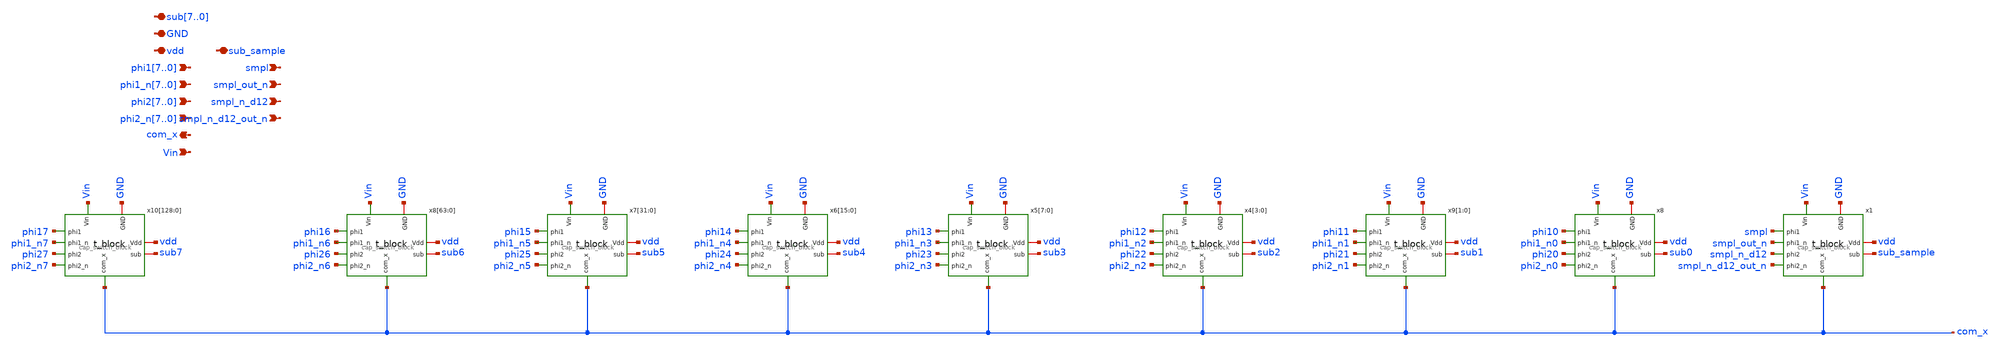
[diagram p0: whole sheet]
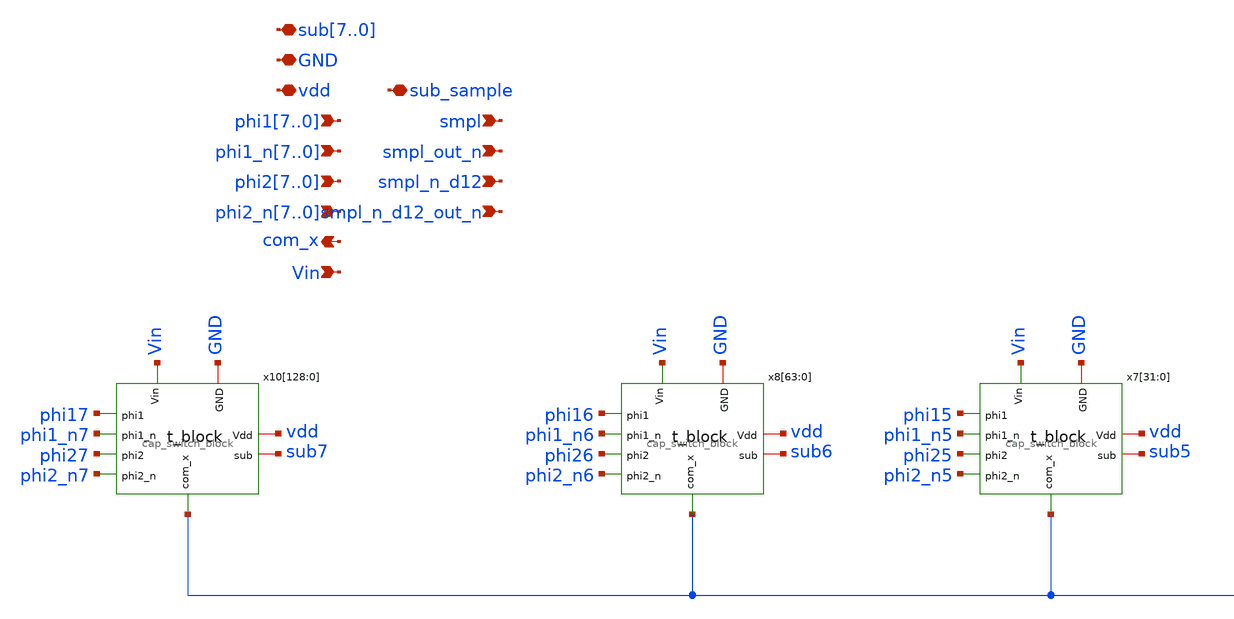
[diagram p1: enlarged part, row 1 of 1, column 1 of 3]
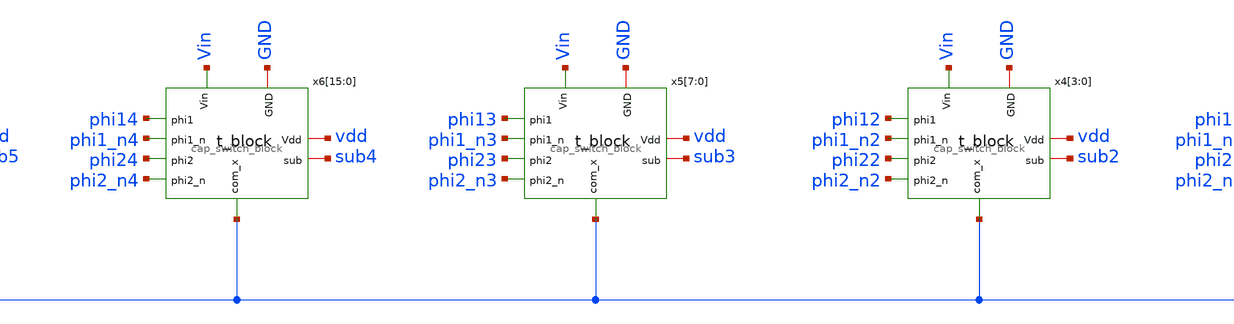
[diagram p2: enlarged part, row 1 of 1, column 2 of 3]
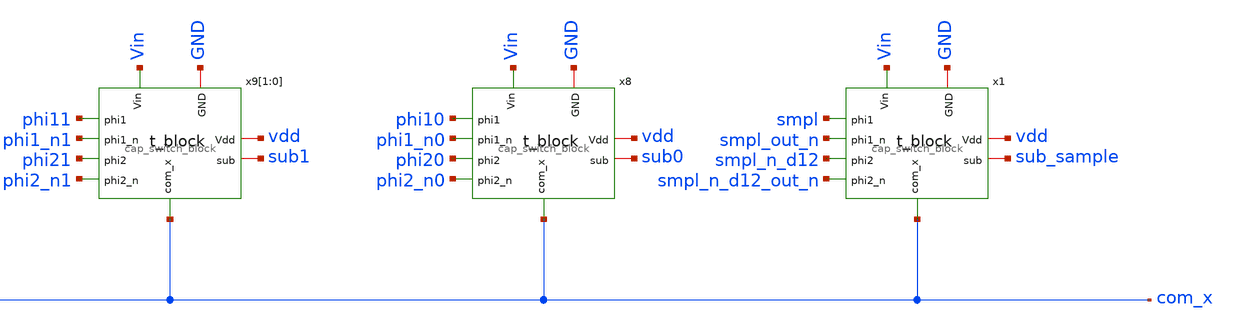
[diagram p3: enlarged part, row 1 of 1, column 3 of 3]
** sch_path: test/design/capblock_256.sch
**.subckt capblock_256 phi17,phi16,phi15,phi14,phi13,phi12,phi11,phi10
*+ phi1_n7,phi1_n6,phi1_n5,phi1_n4,phi1_n3,phi1_n2,phi1_n1,phi1_n0 vdd GND sub7,sub6,sub5,sub4,sub3,sub2,sub1,sub0 phi27,phi26,phi25,phi24,phi23,phi22,phi21,phi20
*+ phi2_n7,phi2_n6,phi2_n5,phi2_n4,phi2_n3,phi2_n2,phi2_n1,phi2_n0 Vin com_x smpl smpl_out_n smpl_n_d12 smpl_n_d12_out_n sub_sample
*.ipin phi17,phi16,phi15,phi14,phi13,phi12,phi11,phi10
*.ipin phi1_n7,phi1_n6,phi1_n5,phi1_n4,phi1_n3,phi1_n2,phi1_n1,phi1_n0
*.iopin vdd
*.iopin GND
*.iopin sub7,sub6,sub5,sub4,sub3,sub2,sub1,sub0
*.ipin phi27,phi26,phi25,phi24,phi23,phi22,phi21,phi20
*.ipin phi2_n7,phi2_n6,phi2_n5,phi2_n4,phi2_n3,phi2_n2,phi2_n1,phi2_n0
*.ipin Vin
*.opin com_x
*.ipin smpl
*.ipin smpl_out_n
*.ipin smpl_n_d12
*.ipin smpl_n_d12_out_n
*.iopin sub_sample
x8 Vin sub0 GND vdd phi10 phi20 phi2_n0 phi1_n0 com_x cap_switch_block
x9[1] Vin sub1 GND vdd phi11 phi21 phi2_n1 phi1_n1 com_x cap_switch_block
x9[0] Vin sub1 GND vdd phi11 phi21 phi2_n1 phi1_n1 com_x cap_switch_block
x4[3] Vin sub2 GND vdd phi12 phi22 phi2_n2 phi1_n2 com_x cap_switch_block
x4[2] Vin sub2 GND vdd phi12 phi22 phi2_n2 phi1_n2 com_x cap_switch_block
x4[1] Vin sub2 GND vdd phi12 phi22 phi2_n2 phi1_n2 com_x cap_switch_block
x4[0] Vin sub2 GND vdd phi12 phi22 phi2_n2 phi1_n2 com_x cap_switch_block
x5[7] Vin sub3 GND vdd phi13 phi23 phi2_n3 phi1_n3 com_x cap_switch_block
x5[6] Vin sub3 GND vdd phi13 phi23 phi2_n3 phi1_n3 com_x cap_switch_block
x5[5] Vin sub3 GND vdd phi13 phi23 phi2_n3 phi1_n3 com_x cap_switch_block
x5[4] Vin sub3 GND vdd phi13 phi23 phi2_n3 phi1_n3 com_x cap_switch_block
x5[3] Vin sub3 GND vdd phi13 phi23 phi2_n3 phi1_n3 com_x cap_switch_block
x5[2] Vin sub3 GND vdd phi13 phi23 phi2_n3 phi1_n3 com_x cap_switch_block
x5[1] Vin sub3 GND vdd phi13 phi23 phi2_n3 phi1_n3 com_x cap_switch_block
x5[0] Vin sub3 GND vdd phi13 phi23 phi2_n3 phi1_n3 com_x cap_switch_block
x6[15] Vin sub4 GND vdd phi14 phi24 phi2_n4 phi1_n4 com_x cap_switch_block
x6[14] Vin sub4 GND vdd phi14 phi24 phi2_n4 phi1_n4 com_x cap_switch_block
x6[13] Vin sub4 GND vdd phi14 phi24 phi2_n4 phi1_n4 com_x cap_switch_block
x6[12] Vin sub4 GND vdd phi14 phi24 phi2_n4 phi1_n4 com_x cap_switch_block
x6[11] Vin sub4 GND vdd phi14 phi24 phi2_n4 phi1_n4 com_x cap_switch_block
x6[10] Vin sub4 GND vdd phi14 phi24 phi2_n4 phi1_n4 com_x cap_switch_block
x6[9] Vin sub4 GND vdd phi14 phi24 phi2_n4 phi1_n4 com_x cap_switch_block
x6[8] Vin sub4 GND vdd phi14 phi24 phi2_n4 phi1_n4 com_x cap_switch_block
x6[7] Vin sub4 GND vdd phi14 phi24 phi2_n4 phi1_n4 com_x cap_switch_block
x6[6] Vin sub4 GND vdd phi14 phi24 phi2_n4 phi1_n4 com_x cap_switch_block
x6[5] Vin sub4 GND vdd phi14 phi24 phi2_n4 phi1_n4 com_x cap_switch_block
x6[4] Vin sub4 GND vdd phi14 phi24 phi2_n4 phi1_n4 com_x cap_switch_block
x6[3] Vin sub4 GND vdd phi14 phi24 phi2_n4 phi1_n4 com_x cap_switch_block
x6[2] Vin sub4 GND vdd phi14 phi24 phi2_n4 phi1_n4 com_x cap_switch_block
x6[1] Vin sub4 GND vdd phi14 phi24 phi2_n4 phi1_n4 com_x cap_switch_block
x6[0] Vin sub4 GND vdd phi14 phi24 phi2_n4 phi1_n4 com_x cap_switch_block
x7[31] Vin sub5 GND vdd phi15 phi25 phi2_n5 phi1_n5 com_x cap_switch_block
x7[30] Vin sub5 GND vdd phi15 phi25 phi2_n5 phi1_n5 com_x cap_switch_block
x7[29] Vin sub5 GND vdd phi15 phi25 phi2_n5 phi1_n5 com_x cap_switch_block
x7[28] Vin sub5 GND vdd phi15 phi25 phi2_n5 phi1_n5 com_x cap_switch_block
x7[27] Vin sub5 GND vdd phi15 phi25 phi2_n5 phi1_n5 com_x cap_switch_block
x7[26] Vin sub5 GND vdd phi15 phi25 phi2_n5 phi1_n5 com_x cap_switch_block
x7[25] Vin sub5 GND vdd phi15 phi25 phi2_n5 phi1_n5 com_x cap_switch_block
x7[24] Vin sub5 GND vdd phi15 phi25 phi2_n5 phi1_n5 com_x cap_switch_block
x7[23] Vin sub5 GND vdd phi15 phi25 phi2_n5 phi1_n5 com_x cap_switch_block
x7[22] Vin sub5 GND vdd phi15 phi25 phi2_n5 phi1_n5 com_x cap_switch_block
x7[21] Vin sub5 GND vdd phi15 phi25 phi2_n5 phi1_n5 com_x cap_switch_block
x7[20] Vin sub5 GND vdd phi15 phi25 phi2_n5 phi1_n5 com_x cap_switch_block
x7[19] Vin sub5 GND vdd phi15 phi25 phi2_n5 phi1_n5 com_x cap_switch_block
x7[18] Vin sub5 GND vdd phi15 phi25 phi2_n5 phi1_n5 com_x cap_switch_block
x7[17] Vin sub5 GND vdd phi15 phi25 phi2_n5 phi1_n5 com_x cap_switch_block
x7[16] Vin sub5 GND vdd phi15 phi25 phi2_n5 phi1_n5 com_x cap_switch_block
x7[15] Vin sub5 GND vdd phi15 phi25 phi2_n5 phi1_n5 com_x cap_switch_block
x7[14] Vin sub5 GND vdd phi15 phi25 phi2_n5 phi1_n5 com_x cap_switch_block
x7[13] Vin sub5 GND vdd phi15 phi25 phi2_n5 phi1_n5 com_x cap_switch_block
x7[12] Vin sub5 GND vdd phi15 phi25 phi2_n5 phi1_n5 com_x cap_switch_block
x7[11] Vin sub5 GND vdd phi15 phi25 phi2_n5 phi1_n5 com_x cap_switch_block
x7[10] Vin sub5 GND vdd phi15 phi25 phi2_n5 phi1_n5 com_x cap_switch_block
x7[9] Vin sub5 GND vdd phi15 phi25 phi2_n5 phi1_n5 com_x cap_switch_block
x7[8] Vin sub5 GND vdd phi15 phi25 phi2_n5 phi1_n5 com_x cap_switch_block
x7[7] Vin sub5 GND vdd phi15 phi25 phi2_n5 phi1_n5 com_x cap_switch_block
x7[6] Vin sub5 GND vdd phi15 phi25 phi2_n5 phi1_n5 com_x cap_switch_block
x7[5] Vin sub5 GND vdd phi15 phi25 phi2_n5 phi1_n5 com_x cap_switch_block
x7[4] Vin sub5 GND vdd phi15 phi25 phi2_n5 phi1_n5 com_x cap_switch_block
x7[3] Vin sub5 GND vdd phi15 phi25 phi2_n5 phi1_n5 com_x cap_switch_block
x7[2] Vin sub5 GND vdd phi15 phi25 phi2_n5 phi1_n5 com_x cap_switch_block
x7[1] Vin sub5 GND vdd phi15 phi25 phi2_n5 phi1_n5 com_x cap_switch_block
x7[0] Vin sub5 GND vdd phi15 phi25 phi2_n5 phi1_n5 com_x cap_switch_block
x8[63] Vin sub6 GND vdd phi16 phi26 phi2_n6 phi1_n6 com_x cap_switch_block
x8[62] Vin sub6 GND vdd phi16 phi26 phi2_n6 phi1_n6 com_x cap_switch_block
x8[61] Vin sub6 GND vdd phi16 phi26 phi2_n6 phi1_n6 com_x cap_switch_block
x8[60] Vin sub6 GND vdd phi16 phi26 phi2_n6 phi1_n6 com_x cap_switch_block
x8[59] Vin sub6 GND vdd phi16 phi26 phi2_n6 phi1_n6 com_x cap_switch_block
x8[58] Vin sub6 GND vdd phi16 phi26 phi2_n6 phi1_n6 com_x cap_switch_block
x8[57] Vin sub6 GND vdd phi16 phi26 phi2_n6 phi1_n6 com_x cap_switch_block
x8[56] Vin sub6 GND vdd phi16 phi26 phi2_n6 phi1_n6 com_x cap_switch_block
x8[55] Vin sub6 GND vdd phi16 phi26 phi2_n6 phi1_n6 com_x cap_switch_block
x8[54] Vin sub6 GND vdd phi16 phi26 phi2_n6 phi1_n6 com_x cap_switch_block
x8[53] Vin sub6 GND vdd phi16 phi26 phi2_n6 phi1_n6 com_x cap_switch_block
x8[52] Vin sub6 GND vdd phi16 phi26 phi2_n6 phi1_n6 com_x cap_switch_block
x8[51] Vin sub6 GND vdd phi16 phi26 phi2_n6 phi1_n6 com_x cap_switch_block
x8[50] Vin sub6 GND vdd phi16 phi26 phi2_n6 phi1_n6 com_x cap_switch_block
x8[49] Vin sub6 GND vdd phi16 phi26 phi2_n6 phi1_n6 com_x cap_switch_block
x8[48] Vin sub6 GND vdd phi16 phi26 phi2_n6 phi1_n6 com_x cap_switch_block
x8[47] Vin sub6 GND vdd phi16 phi26 phi2_n6 phi1_n6 com_x cap_switch_block
x8[46] Vin sub6 GND vdd phi16 phi26 phi2_n6 phi1_n6 com_x cap_switch_block
x8[45] Vin sub6 GND vdd phi16 phi26 phi2_n6 phi1_n6 com_x cap_switch_block
x8[44] Vin sub6 GND vdd phi16 phi26 phi2_n6 phi1_n6 com_x cap_switch_block
x8[43] Vin sub6 GND vdd phi16 phi26 phi2_n6 phi1_n6 com_x cap_switch_block
x8[42] Vin sub6 GND vdd phi16 phi26 phi2_n6 phi1_n6 com_x cap_switch_block
x8[41] Vin sub6 GND vdd phi16 phi26 phi2_n6 phi1_n6 com_x cap_switch_block
x8[40] Vin sub6 GND vdd phi16 phi26 phi2_n6 phi1_n6 com_x cap_switch_block
x8[39] Vin sub6 GND vdd phi16 phi26 phi2_n6 phi1_n6 com_x cap_switch_block
x8[38] Vin sub6 GND vdd phi16 phi26 phi2_n6 phi1_n6 com_x cap_switch_block
x8[37] Vin sub6 GND vdd phi16 phi26 phi2_n6 phi1_n6 com_x cap_switch_block
x8[36] Vin sub6 GND vdd phi16 phi26 phi2_n6 phi1_n6 com_x cap_switch_block
x8[35] Vin sub6 GND vdd phi16 phi26 phi2_n6 phi1_n6 com_x cap_switch_block
x8[34] Vin sub6 GND vdd phi16 phi26 phi2_n6 phi1_n6 com_x cap_switch_block
x8[33] Vin sub6 GND vdd phi16 phi26 phi2_n6 phi1_n6 com_x cap_switch_block
x8[32] Vin sub6 GND vdd phi16 phi26 phi2_n6 phi1_n6 com_x cap_switch_block
x8[31] Vin sub6 GND vdd phi16 phi26 phi2_n6 phi1_n6 com_x cap_switch_block
x8[30] Vin sub6 GND vdd phi16 phi26 phi2_n6 phi1_n6 com_x cap_switch_block
x8[29] Vin sub6 GND vdd phi16 phi26 phi2_n6 phi1_n6 com_x cap_switch_block
x8[28] Vin sub6 GND vdd phi16 phi26 phi2_n6 phi1_n6 com_x cap_switch_block
x8[27] Vin sub6 GND vdd phi16 phi26 phi2_n6 phi1_n6 com_x cap_switch_block
x8[26] Vin sub6 GND vdd phi16 phi26 phi2_n6 phi1_n6 com_x cap_switch_block
x8[25] Vin sub6 GND vdd phi16 phi26 phi2_n6 phi1_n6 com_x cap_switch_block
x8[24] Vin sub6 GND vdd phi16 phi26 phi2_n6 phi1_n6 com_x cap_switch_block
x8[23] Vin sub6 GND vdd phi16 phi26 phi2_n6 phi1_n6 com_x cap_switch_block
x8[22] Vin sub6 GND vdd phi16 phi26 phi2_n6 phi1_n6 com_x cap_switch_block
x8[21] Vin sub6 GND vdd phi16 phi26 phi2_n6 phi1_n6 com_x cap_switch_block
x8[20] Vin sub6 GND vdd phi16 phi26 phi2_n6 phi1_n6 com_x cap_switch_block
x8[19] Vin sub6 GND vdd phi16 phi26 phi2_n6 phi1_n6 com_x cap_switch_block
x8[18] Vin sub6 GND vdd phi16 phi26 phi2_n6 phi1_n6 com_x cap_switch_block
x8[17] Vin sub6 GND vdd phi16 phi26 phi2_n6 phi1_n6 com_x cap_switch_block
x8[16] Vin sub6 GND vdd phi16 phi26 phi2_n6 phi1_n6 com_x cap_switch_block
x8[15] Vin sub6 GND vdd phi16 phi26 phi2_n6 phi1_n6 com_x cap_switch_block
x8[14] Vin sub6 GND vdd phi16 phi26 phi2_n6 phi1_n6 com_x cap_switch_block
x8[13] Vin sub6 GND vdd phi16 phi26 phi2_n6 phi1_n6 com_x cap_switch_block
x8[12] Vin sub6 GND vdd phi16 phi26 phi2_n6 phi1_n6 com_x cap_switch_block
x8[11] Vin sub6 GND vdd phi16 phi26 phi2_n6 phi1_n6 com_x cap_switch_block
x8[10] Vin sub6 GND vdd phi16 phi26 phi2_n6 phi1_n6 com_x cap_switch_block
x8[9] Vin sub6 GND vdd phi16 phi26 phi2_n6 phi1_n6 com_x cap_switch_block
x8[8] Vin sub6 GND vdd phi16 phi26 phi2_n6 phi1_n6 com_x cap_switch_block
x8[7] Vin sub6 GND vdd phi16 phi26 phi2_n6 phi1_n6 com_x cap_switch_block
x8[6] Vin sub6 GND vdd phi16 phi26 phi2_n6 phi1_n6 com_x cap_switch_block
x8[5] Vin sub6 GND vdd phi16 phi26 phi2_n6 phi1_n6 com_x cap_switch_block
x8[4] Vin sub6 GND vdd phi16 phi26 phi2_n6 phi1_n6 com_x cap_switch_block
x8[3] Vin sub6 GND vdd phi16 phi26 phi2_n6 phi1_n6 com_x cap_switch_block
x8[2] Vin sub6 GND vdd phi16 phi26 phi2_n6 phi1_n6 com_x cap_switch_block
x8[1] Vin sub6 GND vdd phi16 phi26 phi2_n6 phi1_n6 com_x cap_switch_block
x8[0] Vin sub6 GND vdd phi16 phi26 phi2_n6 phi1_n6 com_x cap_switch_block
x10[128] Vin sub7 GND vdd phi17 phi27 phi2_n7 phi1_n7 com_x cap_switch_block
x10[127] Vin sub7 GND vdd phi17 phi27 phi2_n7 phi1_n7 com_x cap_switch_block
x10[126] Vin sub7 GND vdd phi17 phi27 phi2_n7 phi1_n7 com_x cap_switch_block
x10[125] Vin sub7 GND vdd phi17 phi27 phi2_n7 phi1_n7 com_x cap_switch_block
x10[124] Vin sub7 GND vdd phi17 phi27 phi2_n7 phi1_n7 com_x cap_switch_block
x10[123] Vin sub7 GND vdd phi17 phi27 phi2_n7 phi1_n7 com_x cap_switch_block
x10[122] Vin sub7 GND vdd phi17 phi27 phi2_n7 phi1_n7 com_x cap_switch_block
x10[121] Vin sub7 GND vdd phi17 phi27 phi2_n7 phi1_n7 com_x cap_switch_block
x10[120] Vin sub7 GND vdd phi17 phi27 phi2_n7 phi1_n7 com_x cap_switch_block
x10[119] Vin sub7 GND vdd phi17 phi27 phi2_n7 phi1_n7 com_x cap_switch_block
x10[118] Vin sub7 GND vdd phi17 phi27 phi2_n7 phi1_n7 com_x cap_switch_block
x10[117] Vin sub7 GND vdd phi17 phi27 phi2_n7 phi1_n7 com_x cap_switch_block
x10[116] Vin sub7 GND vdd phi17 phi27 phi2_n7 phi1_n7 com_x cap_switch_block
x10[115] Vin sub7 GND vdd phi17 phi27 phi2_n7 phi1_n7 com_x cap_switch_block
x10[114] Vin sub7 GND vdd phi17 phi27 phi2_n7 phi1_n7 com_x cap_switch_block
x10[113] Vin sub7 GND vdd phi17 phi27 phi2_n7 phi1_n7 com_x cap_switch_block
x10[112] Vin sub7 GND vdd phi17 phi27 phi2_n7 phi1_n7 com_x cap_switch_block
x10[111] Vin sub7 GND vdd phi17 phi27 phi2_n7 phi1_n7 com_x cap_switch_block
x10[110] Vin sub7 GND vdd phi17 phi27 phi2_n7 phi1_n7 com_x cap_switch_block
x10[109] Vin sub7 GND vdd phi17 phi27 phi2_n7 phi1_n7 com_x cap_switch_block
x10[108] Vin sub7 GND vdd phi17 phi27 phi2_n7 phi1_n7 com_x cap_switch_block
x10[107] Vin sub7 GND vdd phi17 phi27 phi2_n7 phi1_n7 com_x cap_switch_block
x10[106] Vin sub7 GND vdd phi17 phi27 phi2_n7 phi1_n7 com_x cap_switch_block
x10[105] Vin sub7 GND vdd phi17 phi27 phi2_n7 phi1_n7 com_x cap_switch_block
x10[104] Vin sub7 GND vdd phi17 phi27 phi2_n7 phi1_n7 com_x cap_switch_block
x10[103] Vin sub7 GND vdd phi17 phi27 phi2_n7 phi1_n7 com_x cap_switch_block
x10[102] Vin sub7 GND vdd phi17 phi27 phi2_n7 phi1_n7 com_x cap_switch_block
x10[101] Vin sub7 GND vdd phi17 phi27 phi2_n7 phi1_n7 com_x cap_switch_block
x10[100] Vin sub7 GND vdd phi17 phi27 phi2_n7 phi1_n7 com_x cap_switch_block
x10[99] Vin sub7 GND vdd phi17 phi27 phi2_n7 phi1_n7 com_x cap_switch_block
x10[98] Vin sub7 GND vdd phi17 phi27 phi2_n7 phi1_n7 com_x cap_switch_block
x10[97] Vin sub7 GND vdd phi17 phi27 phi2_n7 phi1_n7 com_x cap_switch_block
x10[96] Vin sub7 GND vdd phi17 phi27 phi2_n7 phi1_n7 com_x cap_switch_block
x10[95] Vin sub7 GND vdd phi17 phi27 phi2_n7 phi1_n7 com_x cap_switch_block
x10[94] Vin sub7 GND vdd phi17 phi27 phi2_n7 phi1_n7 com_x cap_switch_block
x10[93] Vin sub7 GND vdd phi17 phi27 phi2_n7 phi1_n7 com_x cap_switch_block
x10[92] Vin sub7 GND vdd phi17 phi27 phi2_n7 phi1_n7 com_x cap_switch_block
x10[91] Vin sub7 GND vdd phi17 phi27 phi2_n7 phi1_n7 com_x cap_switch_block
x10[90] Vin sub7 GND vdd phi17 phi27 phi2_n7 phi1_n7 com_x cap_switch_block
x10[89] Vin sub7 GND vdd phi17 phi27 phi2_n7 phi1_n7 com_x cap_switch_block
x10[88] Vin sub7 GND vdd phi17 phi27 phi2_n7 phi1_n7 com_x cap_switch_block
x10[87] Vin sub7 GND vdd phi17 phi27 phi2_n7 phi1_n7 com_x cap_switch_block
x10[86] Vin sub7 GND vdd phi17 phi27 phi2_n7 phi1_n7 com_x cap_switch_block
x10[85] Vin sub7 GND vdd phi17 phi27 phi2_n7 phi1_n7 com_x cap_switch_block
x10[84] Vin sub7 GND vdd phi17 phi27 phi2_n7 phi1_n7 com_x cap_switch_block
x10[83] Vin sub7 GND vdd phi17 phi27 phi2_n7 phi1_n7 com_x cap_switch_block
x10[82] Vin sub7 GND vdd phi17 phi27 phi2_n7 phi1_n7 com_x cap_switch_block
x10[81] Vin sub7 GND vdd phi17 phi27 phi2_n7 phi1_n7 com_x cap_switch_block
x10[80] Vin sub7 GND vdd phi17 phi27 phi2_n7 phi1_n7 com_x cap_switch_block
x10[79] Vin sub7 GND vdd phi17 phi27 phi2_n7 phi1_n7 com_x cap_switch_block
x10[78] Vin sub7 GND vdd phi17 phi27 phi2_n7 phi1_n7 com_x cap_switch_block
x10[77] Vin sub7 GND vdd phi17 phi27 phi2_n7 phi1_n7 com_x cap_switch_block
x10[76] Vin sub7 GND vdd phi17 phi27 phi2_n7 phi1_n7 com_x cap_switch_block
x10[75] Vin sub7 GND vdd phi17 phi27 phi2_n7 phi1_n7 com_x cap_switch_block
x10[74] Vin sub7 GND vdd phi17 phi27 phi2_n7 phi1_n7 com_x cap_switch_block
x10[73] Vin sub7 GND vdd phi17 phi27 phi2_n7 phi1_n7 com_x cap_switch_block
x10[72] Vin sub7 GND vdd phi17 phi27 phi2_n7 phi1_n7 com_x cap_switch_block
x10[71] Vin sub7 GND vdd phi17 phi27 phi2_n7 phi1_n7 com_x cap_switch_block
x10[70] Vin sub7 GND vdd phi17 phi27 phi2_n7 phi1_n7 com_x cap_switch_block
x10[69] Vin sub7 GND vdd phi17 phi27 phi2_n7 phi1_n7 com_x cap_switch_block
x10[68] Vin sub7 GND vdd phi17 phi27 phi2_n7 phi1_n7 com_x cap_switch_block
x10[67] Vin sub7 GND vdd phi17 phi27 phi2_n7 phi1_n7 com_x cap_switch_block
x10[66] Vin sub7 GND vdd phi17 phi27 phi2_n7 phi1_n7 com_x cap_switch_block
x10[65] Vin sub7 GND vdd phi17 phi27 phi2_n7 phi1_n7 com_x cap_switch_block
x10[64] Vin sub7 GND vdd phi17 phi27 phi2_n7 phi1_n7 com_x cap_switch_block
x10[63] Vin sub7 GND vdd phi17 phi27 phi2_n7 phi1_n7 com_x cap_switch_block
x10[62] Vin sub7 GND vdd phi17 phi27 phi2_n7 phi1_n7 com_x cap_switch_block
x10[61] Vin sub7 GND vdd phi17 phi27 phi2_n7 phi1_n7 com_x cap_switch_block
x10[60] Vin sub7 GND vdd phi17 phi27 phi2_n7 phi1_n7 com_x cap_switch_block
x10[59] Vin sub7 GND vdd phi17 phi27 phi2_n7 phi1_n7 com_x cap_switch_block
x10[58] Vin sub7 GND vdd phi17 phi27 phi2_n7 phi1_n7 com_x cap_switch_block
x10[57] Vin sub7 GND vdd phi17 phi27 phi2_n7 phi1_n7 com_x cap_switch_block
x10[56] Vin sub7 GND vdd phi17 phi27 phi2_n7 phi1_n7 com_x cap_switch_block
x10[55] Vin sub7 GND vdd phi17 phi27 phi2_n7 phi1_n7 com_x cap_switch_block
x10[54] Vin sub7 GND vdd phi17 phi27 phi2_n7 phi1_n7 com_x cap_switch_block
x10[53] Vin sub7 GND vdd phi17 phi27 phi2_n7 phi1_n7 com_x cap_switch_block
x10[52] Vin sub7 GND vdd phi17 phi27 phi2_n7 phi1_n7 com_x cap_switch_block
x10[51] Vin sub7 GND vdd phi17 phi27 phi2_n7 phi1_n7 com_x cap_switch_block
x10[50] Vin sub7 GND vdd phi17 phi27 phi2_n7 phi1_n7 com_x cap_switch_block
x10[49] Vin sub7 GND vdd phi17 phi27 phi2_n7 phi1_n7 com_x cap_switch_block
x10[48] Vin sub7 GND vdd phi17 phi27 phi2_n7 phi1_n7 com_x cap_switch_block
x10[47] Vin sub7 GND vdd phi17 phi27 phi2_n7 phi1_n7 com_x cap_switch_block
x10[46] Vin sub7 GND vdd phi17 phi27 phi2_n7 phi1_n7 com_x cap_switch_block
x10[45] Vin sub7 GND vdd phi17 phi27 phi2_n7 phi1_n7 com_x cap_switch_block
x10[44] Vin sub7 GND vdd phi17 phi27 phi2_n7 phi1_n7 com_x cap_switch_block
x10[43] Vin sub7 GND vdd phi17 phi27 phi2_n7 phi1_n7 com_x cap_switch_block
x10[42] Vin sub7 GND vdd phi17 phi27 phi2_n7 phi1_n7 com_x cap_switch_block
x10[41] Vin sub7 GND vdd phi17 phi27 phi2_n7 phi1_n7 com_x cap_switch_block
x10[40] Vin sub7 GND vdd phi17 phi27 phi2_n7 phi1_n7 com_x cap_switch_block
x10[39] Vin sub7 GND vdd phi17 phi27 phi2_n7 phi1_n7 com_x cap_switch_block
x10[38] Vin sub7 GND vdd phi17 phi27 phi2_n7 phi1_n7 com_x cap_switch_block
x10[37] Vin sub7 GND vdd phi17 phi27 phi2_n7 phi1_n7 com_x cap_switch_block
x10[36] Vin sub7 GND vdd phi17 phi27 phi2_n7 phi1_n7 com_x cap_switch_block
x10[35] Vin sub7 GND vdd phi17 phi27 phi2_n7 phi1_n7 com_x cap_switch_block
x10[34] Vin sub7 GND vdd phi17 phi27 phi2_n7 phi1_n7 com_x cap_switch_block
x10[33] Vin sub7 GND vdd phi17 phi27 phi2_n7 phi1_n7 com_x cap_switch_block
x10[32] Vin sub7 GND vdd phi17 phi27 phi2_n7 phi1_n7 com_x cap_switch_block
x10[31] Vin sub7 GND vdd phi17 phi27 phi2_n7 phi1_n7 com_x cap_switch_block
x10[30] Vin sub7 GND vdd phi17 phi27 phi2_n7 phi1_n7 com_x cap_switch_block
x10[29] Vin sub7 GND vdd phi17 phi27 phi2_n7 phi1_n7 com_x cap_switch_block
x10[28] Vin sub7 GND vdd phi17 phi27 phi2_n7 phi1_n7 com_x cap_switch_block
x10[27] Vin sub7 GND vdd phi17 phi27 phi2_n7 phi1_n7 com_x cap_switch_block
x10[26] Vin sub7 GND vdd phi17 phi27 phi2_n7 phi1_n7 com_x cap_switch_block
x10[25] Vin sub7 GND vdd phi17 phi27 phi2_n7 phi1_n7 com_x cap_switch_block
x10[24] Vin sub7 GND vdd phi17 phi27 phi2_n7 phi1_n7 com_x cap_switch_block
x10[23] Vin sub7 GND vdd phi17 phi27 phi2_n7 phi1_n7 com_x cap_switch_block
x10[22] Vin sub7 GND vdd phi17 phi27 phi2_n7 phi1_n7 com_x cap_switch_block
x10[21] Vin sub7 GND vdd phi17 phi27 phi2_n7 phi1_n7 com_x cap_switch_block
x10[20] Vin sub7 GND vdd phi17 phi27 phi2_n7 phi1_n7 com_x cap_switch_block
x10[19] Vin sub7 GND vdd phi17 phi27 phi2_n7 phi1_n7 com_x cap_switch_block
x10[18] Vin sub7 GND vdd phi17 phi27 phi2_n7 phi1_n7 com_x cap_switch_block
x10[17] Vin sub7 GND vdd phi17 phi27 phi2_n7 phi1_n7 com_x cap_switch_block
x10[16] Vin sub7 GND vdd phi17 phi27 phi2_n7 phi1_n7 com_x cap_switch_block
x10[15] Vin sub7 GND vdd phi17 phi27 phi2_n7 phi1_n7 com_x cap_switch_block
x10[14] Vin sub7 GND vdd phi17 phi27 phi2_n7 phi1_n7 com_x cap_switch_block
x10[13] Vin sub7 GND vdd phi17 phi27 phi2_n7 phi1_n7 com_x cap_switch_block
x10[12] Vin sub7 GND vdd phi17 phi27 phi2_n7 phi1_n7 com_x cap_switch_block
x10[11] Vin sub7 GND vdd phi17 phi27 phi2_n7 phi1_n7 com_x cap_switch_block
x10[10] Vin sub7 GND vdd phi17 phi27 phi2_n7 phi1_n7 com_x cap_switch_block
x10[9] Vin sub7 GND vdd phi17 phi27 phi2_n7 phi1_n7 com_x cap_switch_block
x10[8] Vin sub7 GND vdd phi17 phi27 phi2_n7 phi1_n7 com_x cap_switch_block
x10[7] Vin sub7 GND vdd phi17 phi27 phi2_n7 phi1_n7 com_x cap_switch_block
x10[6] Vin sub7 GND vdd phi17 phi27 phi2_n7 phi1_n7 com_x cap_switch_block
x10[5] Vin sub7 GND vdd phi17 phi27 phi2_n7 phi1_n7 com_x cap_switch_block
x10[4] Vin sub7 GND vdd phi17 phi27 phi2_n7 phi1_n7 com_x cap_switch_block
x10[3] Vin sub7 GND vdd phi17 phi27 phi2_n7 phi1_n7 com_x cap_switch_block
x10[2] Vin sub7 GND vdd phi17 phi27 phi2_n7 phi1_n7 com_x cap_switch_block
x10[1] Vin sub7 GND vdd phi17 phi27 phi2_n7 phi1_n7 com_x cap_switch_block
x10[0] Vin sub7 GND vdd phi17 phi27 phi2_n7 phi1_n7 com_x cap_switch_block
x1 Vin sub_sample GND vdd smpl smpl_n_d12 smpl_n_d12_out_n smpl_out_n com_x cap_switch_block
**.ends

* expanding   symbol:  cap_switch_block.sym # of pins=9
** sym_path: test/design/cap_switch_block.sym
** sch_path: test/design/cap_switch_block.sch
.subckt cap_switch_block Vin sub GND Vdd phi1 phi2 phi2_n phi1_n com_x
*.ipin Vin
*.opin com_x
*.ipin phi1
*.ipin phi1_n
*.iopin Vdd
*.iopin GND
*.iopin sub
*.ipin phi2
*.ipin phi2_n
XC9 com_x net1 sky130_fd_pr__cap_mim_m3_1 W=7 L=7 MF=1 m=1
x4 phi1 sub net1 Vin Vdd phi1_n tg_final
x1 phi2 sub net1 GND Vdd phi2_n tg_final
.ends


* expanding   symbol:  final/tg_final.sym # of pins=6
** sym_path: top/test/design/tg_final.sym
** sch_path: top/test/design/tg_final.sch
.subckt tg_final clk sub vout vin vdd clk_b
*.ipin clk
*.ipin vin
*.opin vout
*.ipin vdd
*.ipin sub
*.ipin clk_b
XM2 vout clk vin sub sky130_fd_pr__nfet_01v8 L=0.15 W=1 nf=1 ad='int((nf+1)/2) * W/nf * 0.29' as='int((nf+2)/2) * W/nf * 0.29'
+ pd='2*int((nf+1)/2) * (W/nf + 0.29)' ps='2*int((nf+2)/2) * (W/nf + 0.29)' nrd='0.29 / W' nrs='0.29 / W'
+ sa=0 sb=0 sd=0 mult=1 m=1
XM1 vout clk_b vin vdd sky130_fd_pr__pfet_01v8 L=0.15 W=1 nf=1 ad='int((nf+1)/2) * W/nf * 0.29' as='int((nf+2)/2) * W/nf * 0.29'
+ pd='2*int((nf+1)/2) * (W/nf + 0.29)' ps='2*int((nf+2)/2) * (W/nf + 0.29)' nrd='0.29 / W' nrs='0.29 / W'
+ sa=0 sb=0 sd=0 mult=1 m=1
.ends

.end
